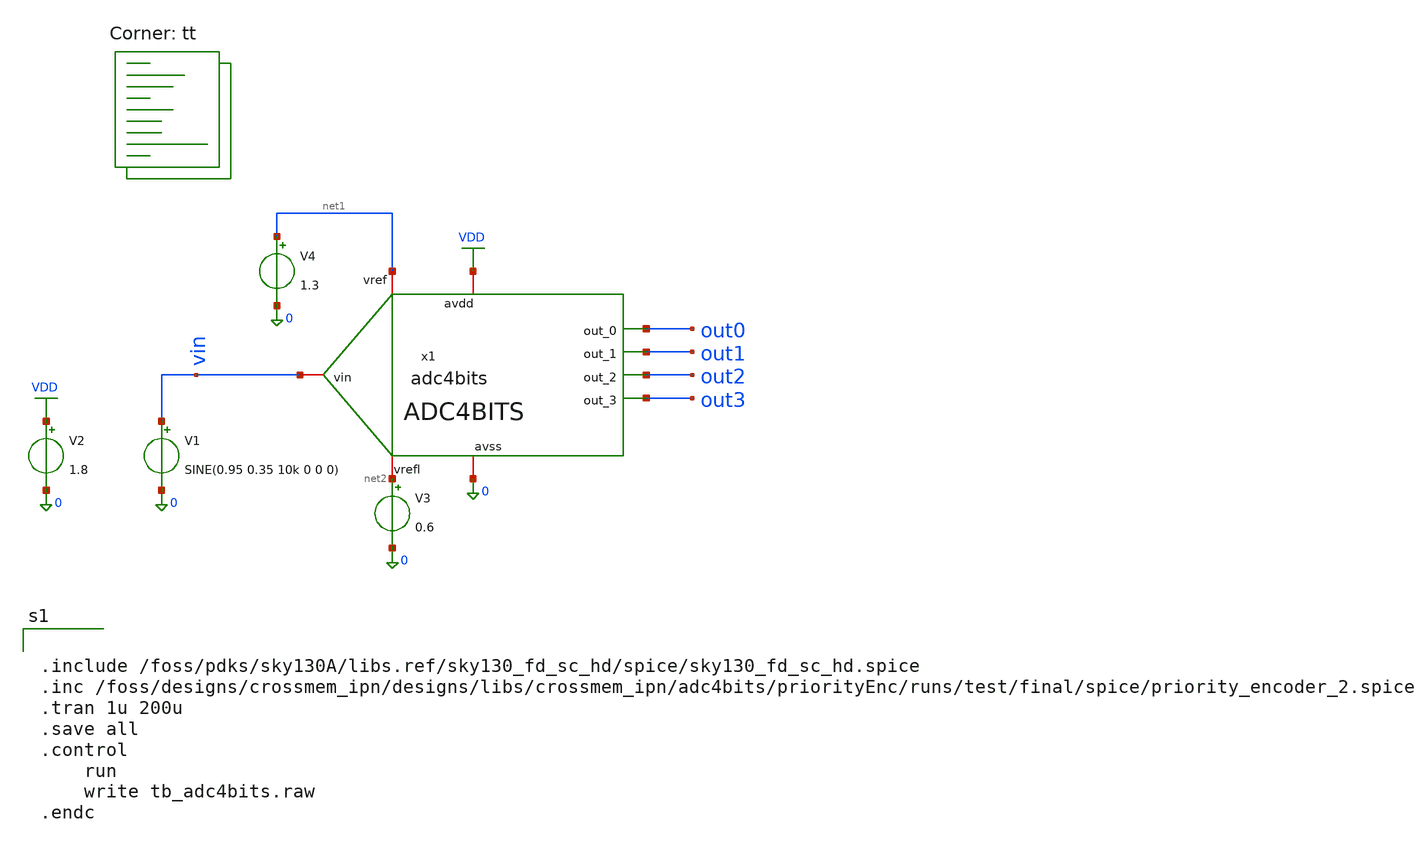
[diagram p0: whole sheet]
** sch_path: designs/libs/crossmem_ipn/adc4bits/tb_adc4bits.sch
**.subckt tb_adc4bits
V1 vin 0 SINE(0.95 0.35 10k 0 0 0)
x1 vin net1 out0 out1 out2 out3 0 VDD net2 adc4bits
V2 VDD 0 1.8
V3 net2 0 0.6
V4 net1 0 1.3
**** begin user architecture code


.include /foss/pdks/sky130A/libs.ref/sky130_fd_sc_hd/spice/sky130_fd_sc_hd.spice
.inc /foss/designs/crossmem_ipn/designs/libs/crossmem_ipn/adc4bits/priorityEnc/runs/test/final/spice/priority_encoder_2.spice
.tran 1u 200u
.save all
.control
	run
	write tb_adc4bits.raw
.endc


.lib $::SKYWATER_MODELS/sky130.lib.spice tt
**** end user architecture code
**.ends

* expanding   symbol:  adc4bits.sym # of pins=9
** sym_path: designs/libs/crossmem_ipn/adc4bits/adc4bits.sym
** sch_path: designs/libs/crossmem_ipn/adc4bits/adc4bits.sch
.subckt adc4bits vin vref out_0 out_1 out_2 out_3 avss avdd vrefl
*.iopin vref
*.iopin avss
*.iopin vin
*.opin out_0
*.opin out_1
*.opin out_2
*.opin out_3
*.iopin avdd
*.iopin vrefl
x1 avdd vin vref n1 avss opamp
x2 avdd vin v1 n2 avss opamp
x3 avdd vin v2 n3 avss opamp
x4 avdd vin v3 n4 avss opamp
x5 avdd vin v4 n5 avss opamp
x6 avdd vin v5 n6 avss opamp
x7 avdd vin v6 n7 avss opamp
x8 avdd vin v7 n8 avss opamp
x9 avdd vin v8 n9 avss opamp
x10 avdd vin v9 n10 avss opamp
x11 avdd vin v10 n11 avss opamp
x12 avdd vin v11 n12 avss opamp
x13 avdd vin v12 n13 avss opamp
x14 avdd vin v13 n14 avss opamp
x15 avdd vin v14 n15 avss opamp
x16 avss avdd n1 n11 n12 n13 n14 n15 avss n2 n3 n4 n5 n6 n7 n8 n9 n10 out_0 out_1 out_2 out_3
+ priority_encoder
R1 v1 vref sky130_fd_pr__res_generic_l1 W=1 L=3.75 m=1
R2 v2 v1 sky130_fd_pr__res_generic_l1 W=1 L=3.75 m=1
R3 v3 v2 sky130_fd_pr__res_generic_l1 W=1 L=3.75 m=1
R4 v4 v3 sky130_fd_pr__res_generic_l1 W=1 L=3.75 m=1
R5 v5 v4 sky130_fd_pr__res_generic_l1 W=1 L=3.75 m=1
R6 v6 v5 sky130_fd_pr__res_generic_l1 W=1 L=3.75 m=1
R7 v7 v6 sky130_fd_pr__res_generic_l1 W=1 L=3.75 m=1
R8 v8 v7 sky130_fd_pr__res_generic_l1 W=1 L=3.75 m=1
R9 v9 v8 sky130_fd_pr__res_generic_l1 W=1 L=3.75 m=1
R10 v10 v9 sky130_fd_pr__res_generic_l1 W=1 L=3.75 m=1
R11 v11 v10 sky130_fd_pr__res_generic_l1 W=1 L=3.75 m=1
R12 v12 v11 sky130_fd_pr__res_generic_l1 W=1 L=3.75 m=1
R13 v13 v12 sky130_fd_pr__res_generic_l1 W=1 L=3.75 m=1
R14 v14 v13 sky130_fd_pr__res_generic_l1 W=1 L=3.75 m=1
R15 vrefl v14 sky130_fd_pr__res_generic_l1 W=1 L=3.75 m=1
.ends


* expanding   symbol:  /foss/designs/crossmem_ipn/designs/libs/crossmem_ipn/opamp/opamp.sym # of
*+ pins=5
** sym_path: designs/libs/crossmem_ipn/opamp/opamp.sym
** sch_path: designs/libs/crossmem_ipn/opamp/opamp.sch
.subckt opamp vdd vin1 vin2 vout vss
*.iopin vss
*.iopin vdd
*.opin vout
*.ipin vin1
*.ipin vin2
XM3 net1 net1 vdd vdd sky130_fd_pr__pfet_01v8 L=1 W=9 nf=1 ad='int((1 + 1)/2) * 9 / 1 * 0.29' as='int((1 + 2)/2) * 9 / 1 * 0.29'
+ pd='2*int((1 + 1)/2) * (9 / 1 + 0.29)' ps='2*int((1 + 2)/2) * (9 / 1 + 0.29)' nrd='0.29 / 9 ' nrs='0.29 / 9 '
+ sa=0 sb=0 sd=0 mult=1 m=1
XM4 net2 net1 vdd vdd sky130_fd_pr__pfet_01v8 L=1 W=9 nf=1 ad='int((1 + 1)/2) * 9 / 1 * 0.29' as='int((1 + 2)/2) * 9 / 1 * 0.29'
+ pd='2*int((1 + 1)/2) * (9 / 1 + 0.29)' ps='2*int((1 + 2)/2) * (9 / 1 + 0.29)' nrd='0.29 / 9 ' nrs='0.29 / 9 '
+ sa=0 sb=0 sd=0 mult=1 m=1
XM6 vout net2 vdd vdd sky130_fd_pr__pfet_01v8 L=1 W=8.65 nf=20 ad='int((20 + 1)/2) * 8.65 / 20 * 0.29'
+ as='int((20 + 2)/2) * 8.65 / 20 * 0.29' pd='2*int((20 + 1)/2) * (8.65 / 20 + 0.29)' ps='2*int((20 + 2)/2) * (8.65 / 20 + 0.29)'
+ nrd='0.29 / 8.65 ' nrs='0.29 / 8.65 ' sa=0 sb=0 sd=0 mult=1 m=1
XM1 net1 vin1 net3 vss sky130_fd_pr__nfet_01v8 L=1 W=5 nf=1 ad='int((1 + 1)/2) * 5 / 1 * 0.29' as='int((1 + 2)/2) * 5 / 1 * 0.29'
+ pd='2*int((1 + 1)/2) * (5 / 1 + 0.29)' ps='2*int((1 + 2)/2) * (5 / 1 + 0.29)' nrd='0.29 / 5 ' nrs='0.29 / 5 '
+ sa=0 sb=0 sd=0 mult=1 m=1
XM2 net2 vin2 net3 vss sky130_fd_pr__nfet_01v8 L=1 W=5 nf=1 ad='int((1 + 1)/2) * 5 / 1 * 0.29' as='int((1 + 2)/2) * 5 / 1 * 0.29'
+ pd='2*int((1 + 1)/2) * (5 / 1 + 0.29)' ps='2*int((1 + 2)/2) * (5 / 1 + 0.29)' nrd='0.29 / 5 ' nrs='0.29 / 5 '
+ sa=0 sb=0 sd=0 mult=1 m=1
XM5 net3 vb1 vss vss sky130_fd_pr__nfet_01v8 L=1 W=8 nf=1 ad='int((1 + 1)/2) * 8 / 1 * 0.29' as='int((1 + 2)/2) * 8 / 1 * 0.29'
+ pd='2*int((1 + 1)/2) * (8 / 1 + 0.29)' ps='2*int((1 + 2)/2) * (8 / 1 + 0.29)' nrd='0.29 / 8 ' nrs='0.29 / 8 '
+ sa=0 sb=0 sd=0 mult=1 m=1
XM8 vb1 vb1 vss vss sky130_fd_pr__nfet_01v8 L=1 W=8 nf=1 ad='int((1 + 1)/2) * 8 / 1 * 0.29' as='int((1 + 2)/2) * 8 / 1 * 0.29'
+ pd='2*int((1 + 1)/2) * (8 / 1 + 0.29)' ps='2*int((1 + 2)/2) * (8 / 1 + 0.29)' nrd='0.29 / 8 ' nrs='0.29 / 8 '
+ sa=0 sb=0 sd=0 mult=1 m=1
XM7 vout vb1 vss vss sky130_fd_pr__nfet_01v8 L=1 W=7 nf=16 ad='int((16 + 1)/2) * 7 / 16 * 0.29' as='int((16 + 2)/2) * 7 / 16 * 0.29'
+ pd='2*int((16 + 1)/2) * (7 / 16 + 0.29)' ps='2*int((16 + 2)/2) * (7 / 16 + 0.29)' nrd='0.29 / 7 ' nrs='0.29 / 7 '
+ sa=0 sb=0 sd=0 mult=1 m=1
XC1 net2 vout sky130_fd_pr__cap_mim_m3_1 W=30 L=30 MF=1 m=1
XM9 vb1 vb1 vdd vdd sky130_fd_pr__pfet_01v8 L=0.5 W=0.5 nf=1 ad='int((1 + 1)/2) * 0.5 / 1 * 0.29' as='int((1 + 2)/2) * 0.5 / 1 * 0.29'
+ pd='2*int((1 + 1)/2) * (0.5 / 1 + 0.29)' ps='2*int((1 + 2)/2) * (0.5 / 1 + 0.29)' nrd='0.29 / 0.5 ' nrs='0.29 / 0.5 '
+ sa=0 sb=0 sd=0 mult=1 m=1
.ends

.GLOBAL VDD
.end
